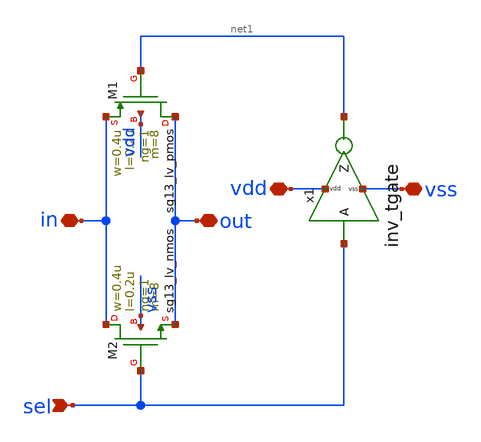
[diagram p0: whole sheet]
** sch_path: v2_feature_extr_withf/tgate.sch
**.subckt tgate vdd vss in out sel
*.iopin vdd
*.iopin vss
*.iopin in
*.iopin out
*.ipin sel
XM1 out net1 in vdd sg13_lv_pmos w=0.4u l=0.2u ng=1 m=8 mm_ok=1
XM2 in sel out vss sg13_lv_nmos w=0.4u l=0.2u ng=1 m=8 mm_ok=1
x1 vdd sel net1 vss inv_tgate
**.ends
.end
